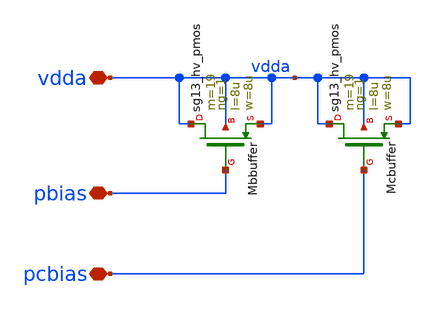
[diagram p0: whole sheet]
** sch_path: xschem/analog_wires.sch
**.subckt analog_wires vdda pcbias pbias
*.iopin vdda
*.iopin pcbias
*.iopin pbias
XMcbuffer vdda pcbias vdda vdda sg13_hv_pmos w=8u l=8u ng=1 m=19 mm_ok=1
XMbbuffer vdda pbias vdda vdda sg13_hv_pmos w=8u l=8u ng=1 m=19 mm_ok=1
**.ends
.end
